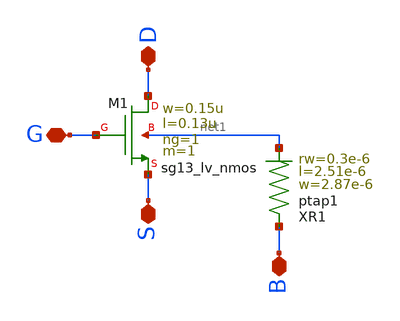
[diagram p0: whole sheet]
** sch_path: ihp-sg13cmos5l/schematic/xschem/sg13_lv_nmos_ring_dev.sch
**.subckt sg13_lv_nmos_ring_dev D S G B
*.iopin D
*.iopin S
*.iopin G
*.iopin B
XM1 D G S net1 sg13_lv_nmos w=0.15u l=0.13u ng=1 m=1 mm_ok=1
XR1 B net1 ptap1 R=23.84 w=2.87e-6 l=2.51e-6 rw=0.3e-6
**.ends
.end
